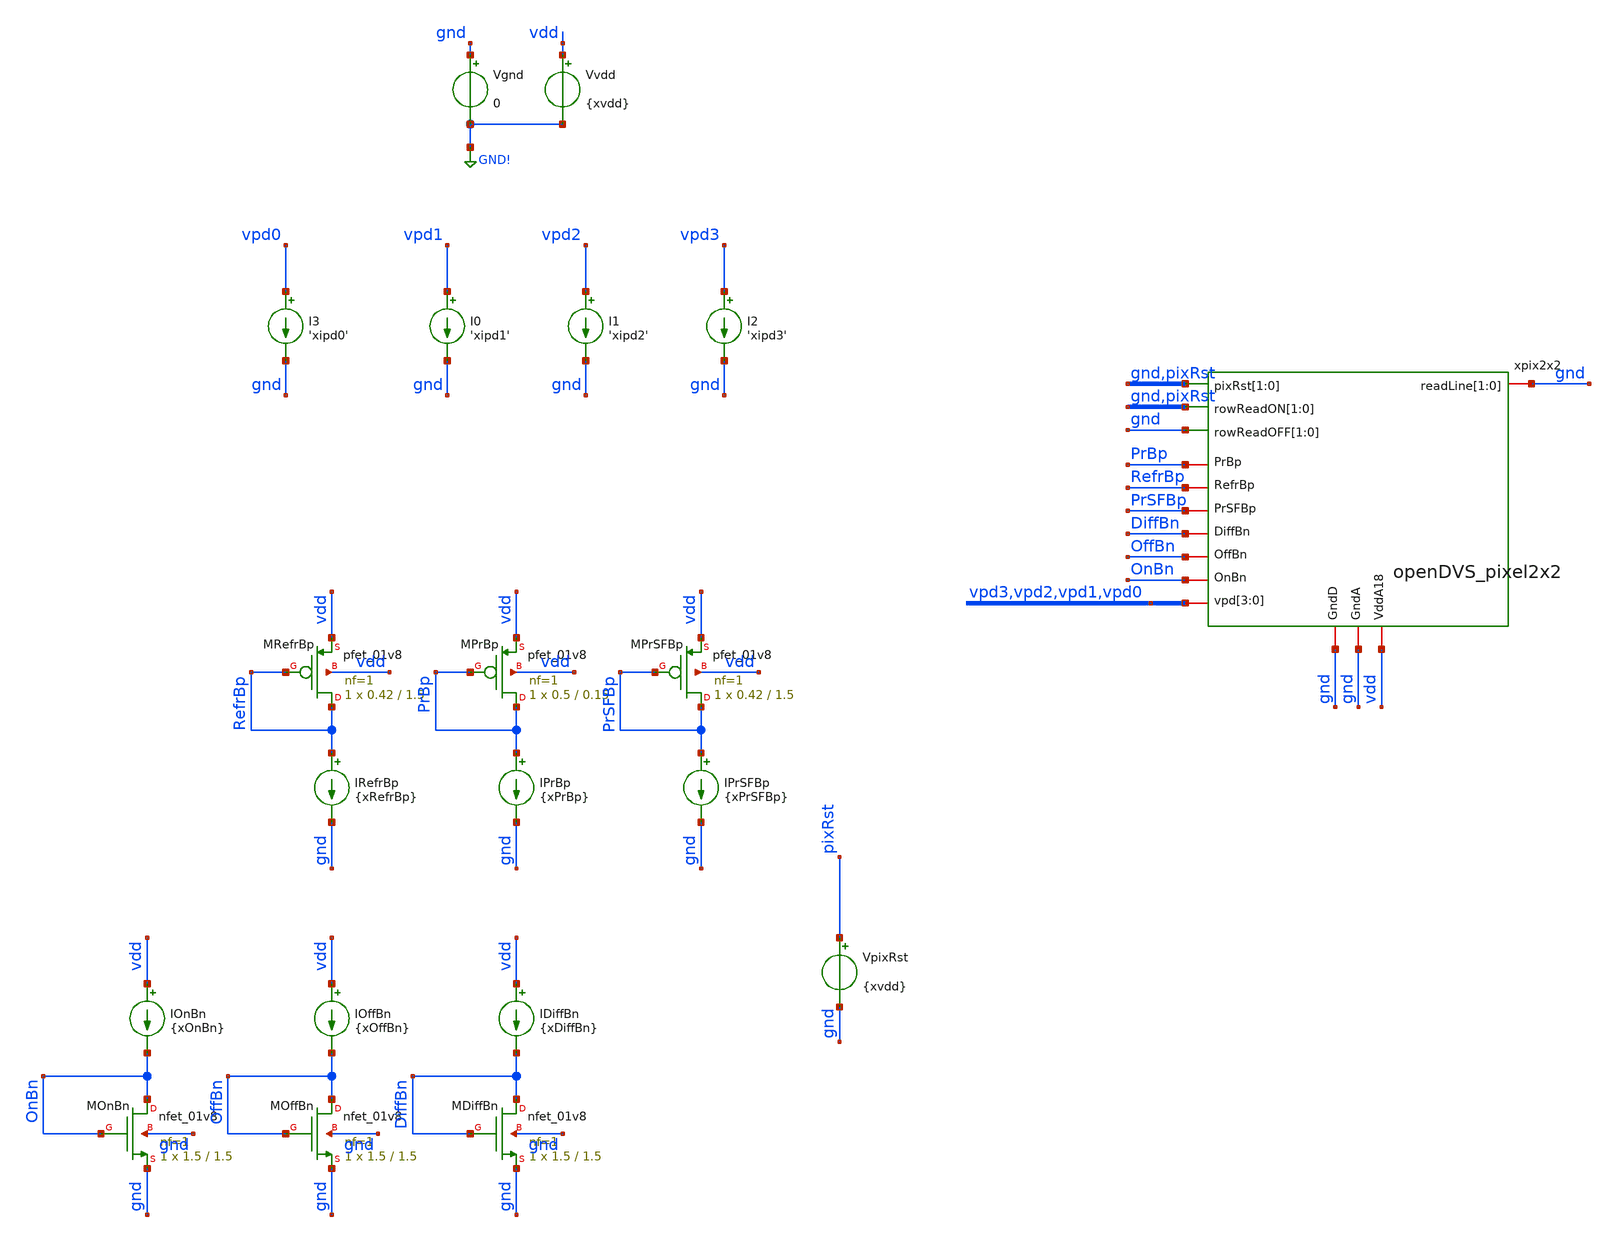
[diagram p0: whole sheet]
** sch_path: analog/xschem/tb_PixelReset_tran_2x2.sch
**.subckt tb_PixelReset_tran_2x2
IRefrBp RefrBp gnd {xRefrBp}
XMRefrBp RefrBp RefrBp vdd vdd sky130_fd_pr__pfet_01v8 L=1.5 W=0.42 nf=1 ad='int((1 + 1)/2) * 0.42 / 1 * 0.29'
+ as='int((1 + 2)/2) * 0.42 / 1 * 0.29' pd='2*int((1 + 1)/2) * (0.42 / 1 + 0.29)' ps='2*int((1 + 2)/2) * (0.42 / 1 + 0.29)'
+ nrd='0.29 / 0.42 ' nrs='0.29 / 0.42 ' sa=0 sb=0 sd=0 mult=1 m=1
XMOnBn OnBn OnBn gnd gnd sky130_fd_pr__nfet_01v8 L=1.5 W=1.5 nf=1 ad='int((1 + 1)/2) * 1.5 / 1 * 0.29'
+ as='int((1 + 2)/2) * 1.5 / 1 * 0.29' pd='2*int((1 + 1)/2) * (1.5 / 1 + 0.29)' ps='2*int((1 + 2)/2) * (1.5 / 1 + 0.29)'
+ nrd='0.29 / 1.5 ' nrs='0.29 / 1.5 ' sa=0 sb=0 sd=0 mult=1 m=1
IOnBn vdd OnBn {xOnBn}
XMOffBn OffBn OffBn gnd gnd sky130_fd_pr__nfet_01v8 L=1.5 W=1.5 nf=1 ad='int((1 + 1)/2) * 1.5 / 1 * 0.29'
+ as='int((1 + 2)/2) * 1.5 / 1 * 0.29' pd='2*int((1 + 1)/2) * (1.5 / 1 + 0.29)' ps='2*int((1 + 2)/2) * (1.5 / 1 + 0.29)'
+ nrd='0.29 / 1.5 ' nrs='0.29 / 1.5 ' sa=0 sb=0 sd=0 mult=1 m=1
IOffBn vdd OffBn {xOffBn}
VpixRst pixRst gnd {xvdd}
xpix2x2 gnd pixRst gnd pixRst gnd gnd gnd gnd vpd3 vpd2 vpd1 vpd0 vdd gnd gnd OnBn OffBn DiffBn
+ PrSFBp RefrBp PrBp openDVS_pixel2x2
I0 vpd1 gnd 'xipd1'
I1 vpd2 gnd 'xipd2'
I2 vpd3 gnd 'xipd3'
I3 vpd0 gnd 'xipd0'
XMPrBp PrBp PrBp vdd vdd sky130_fd_pr__pfet_01v8 L=0.15 W=0.5 nf=1 ad='int((1 + 1)/2) * 0.5 / 1 * 0.29'
+ as='int((1 + 2)/2) * 0.5 / 1 * 0.29' pd='2*int((1 + 1)/2) * (0.5 / 1 + 0.29)' ps='2*int((1 + 2)/2) * (0.5 / 1 + 0.29)'
+ nrd='0.29 / 0.5 ' nrs='0.29 / 0.5 ' sa=0 sb=0 sd=0 mult=1 m=1
IPrBp PrBp gnd {xPrBp}
XMPrSFBp PrSFBp PrSFBp vdd vdd sky130_fd_pr__pfet_01v8 L=1.5 W=0.42 nf=1 ad='int((1 + 1)/2) * 0.42 / 1 * 0.29'
+ as='int((1 + 2)/2) * 0.42 / 1 * 0.29' pd='2*int((1 + 1)/2) * (0.42 / 1 + 0.29)' ps='2*int((1 + 2)/2) * (0.42 / 1 + 0.29)'
+ nrd='0.29 / 0.42 ' nrs='0.29 / 0.42 ' sa=0 sb=0 sd=0 mult=1 m=1
IPrSFBp PrSFBp gnd {xPrSFBp}
XMDiffBn DiffBn DiffBn gnd gnd sky130_fd_pr__nfet_01v8 L=1.5 W=1.5 nf=1 ad='int((1 + 1)/2) * 1.5 / 1 * 0.29'
+ as='int((1 + 2)/2) * 1.5 / 1 * 0.29' pd='2*int((1 + 1)/2) * (1.5 / 1 + 0.29)' ps='2*int((1 + 2)/2) * (1.5 / 1 + 0.29)'
+ nrd='0.29 / 1.5 ' nrs='0.29 / 1.5 ' sa=0 sb=0 sd=0 mult=1 m=1
IDiffBn vdd DiffBn {xDiffBn}
Vgnd gnd GND! 0
Vvdd vdd GND! {xvdd}
**** begin user architecture code

** opencircuitdesign pdks install
.lib $::SKYWATER_MODELS/sky130.lib.spice tt



.temp 27

** PEX netlist includes — uncomment one
*.include /home/rpgraca/research/projects/telluride/2025/nic_eventcam/nic2025_openDVS/analog/xschem/openDVS_pixel2x2_pex_simple.spice
*.include /home/rpgraca/research/projects/telluride/2025/nic_eventcam/nic2025_openDVS/analog/xschem/openDVS_pixel2x2_pex_r.spice
*.include /home/rpgraca/research/projects/telluride/2025/nic_eventcam/nic2025_openDVS/analog/xschem/openDVS_pixel2x2_pex_cc.spice
*.include /home/rpgraca/research/projects/telluride/2025/nic_eventcam/nic2025_openDVS/analog/xschem/openDVS_pixel2x2_pex_c.spice
.include /home/rpgraca/research/projects/telluride/2025/nic_eventcam/nic2025_openDVS/analog/xschem/openDVS_pixel2x2_pex_rcc.spice
*.include /home/rpgraca/research/projects/telluride/2025/nic_eventcam/nic2025_openDVS/analog/xschem/openDVS_pixel2x2_pex_rc.spice

.option gmin=1e-17 abstol=1e-15 vntol=1e-9 reltol=1e-4 chgtol=1e-16
.option method=gear maxord=2 trtol=1
.option itl1=500 itl2=200 itl4=50
.option gminsteps=200 srcsteps=200
.option ramptime=100n

.param xvdd = 1.8
.param xPrBp = 10n
.param xPrSFBp = 100p
.param xDiffBn = 5n
.param xRefrBp = 400p
.param xOnBn = 200n
.param xOffBn = 0.25n

.param xipd0 = 1n
.param xipd1 = 1n
.param xipd2 = 1n
.param xipd3 = 1n

.save all

** Bsource probes: mirror internal nodes to top-level names (brackets OK in SPICE deck)
Bprobe_on on_mon 0 V = v(xpix2x2.pix[0].on)
Bprobe_nrst nrst_mon 0 V = v(xpix2x2.pix[0].nrst)
Bprobe_vdiff vdiff_mon 0 V = v(xpix2x2.pix[0].vdiff)

.control
** Phase 1: initial reset (VpixRst = xvdd, DC source)
stop when time > 1m
tran 100u 50
let vdd_val = v(vdd)[length(v(vdd))-1]
echo
echo '=== Phase 1: initial reset complete (t=1ms) ==='

** Phase 2: release reset, run until ON fires
alter vpixrst = 0
delete all
let on_thresh = 0.9 * vdd_val
stop when v(on_mon) > $&on_thresh
resume

let t_on_event = time[length(time)-1]
echo
echo '=== Phase 2: ON event detected ==='
print t_on_event

** Phase 3: trigger second reset for 10us
alter vpixrst = $&vdd_val
delete all
let t_rst2_end = t_on_event + 10u
stop when time > $&t_rst2_end
resume
echo
echo '=== Phase 3: second reset complete (10us pulse) ==='

** Phase 4: release second reset, run 0.5s more
alter vpixrst = 0
delete all
let t_final = t_on_event + 0.5
stop when time > $&t_final
resume
echo
echo '=== Phase 4: post-reset observation complete ==='

write tb_PixelReset_tran_2x2.raw
echo 'Raw file written. Running Python analysis...'
shell python3
+ /home/rpgraca/research/projects/telluride/2025/nic_eventcam/nic2025_openDVS/analog/xschem/process_PixelReset_tran_2x2.py tb_PixelReset_tran_2x2.raw
.endc


**** end user architecture code
**.ends
.GLOBAL GND!
.end
